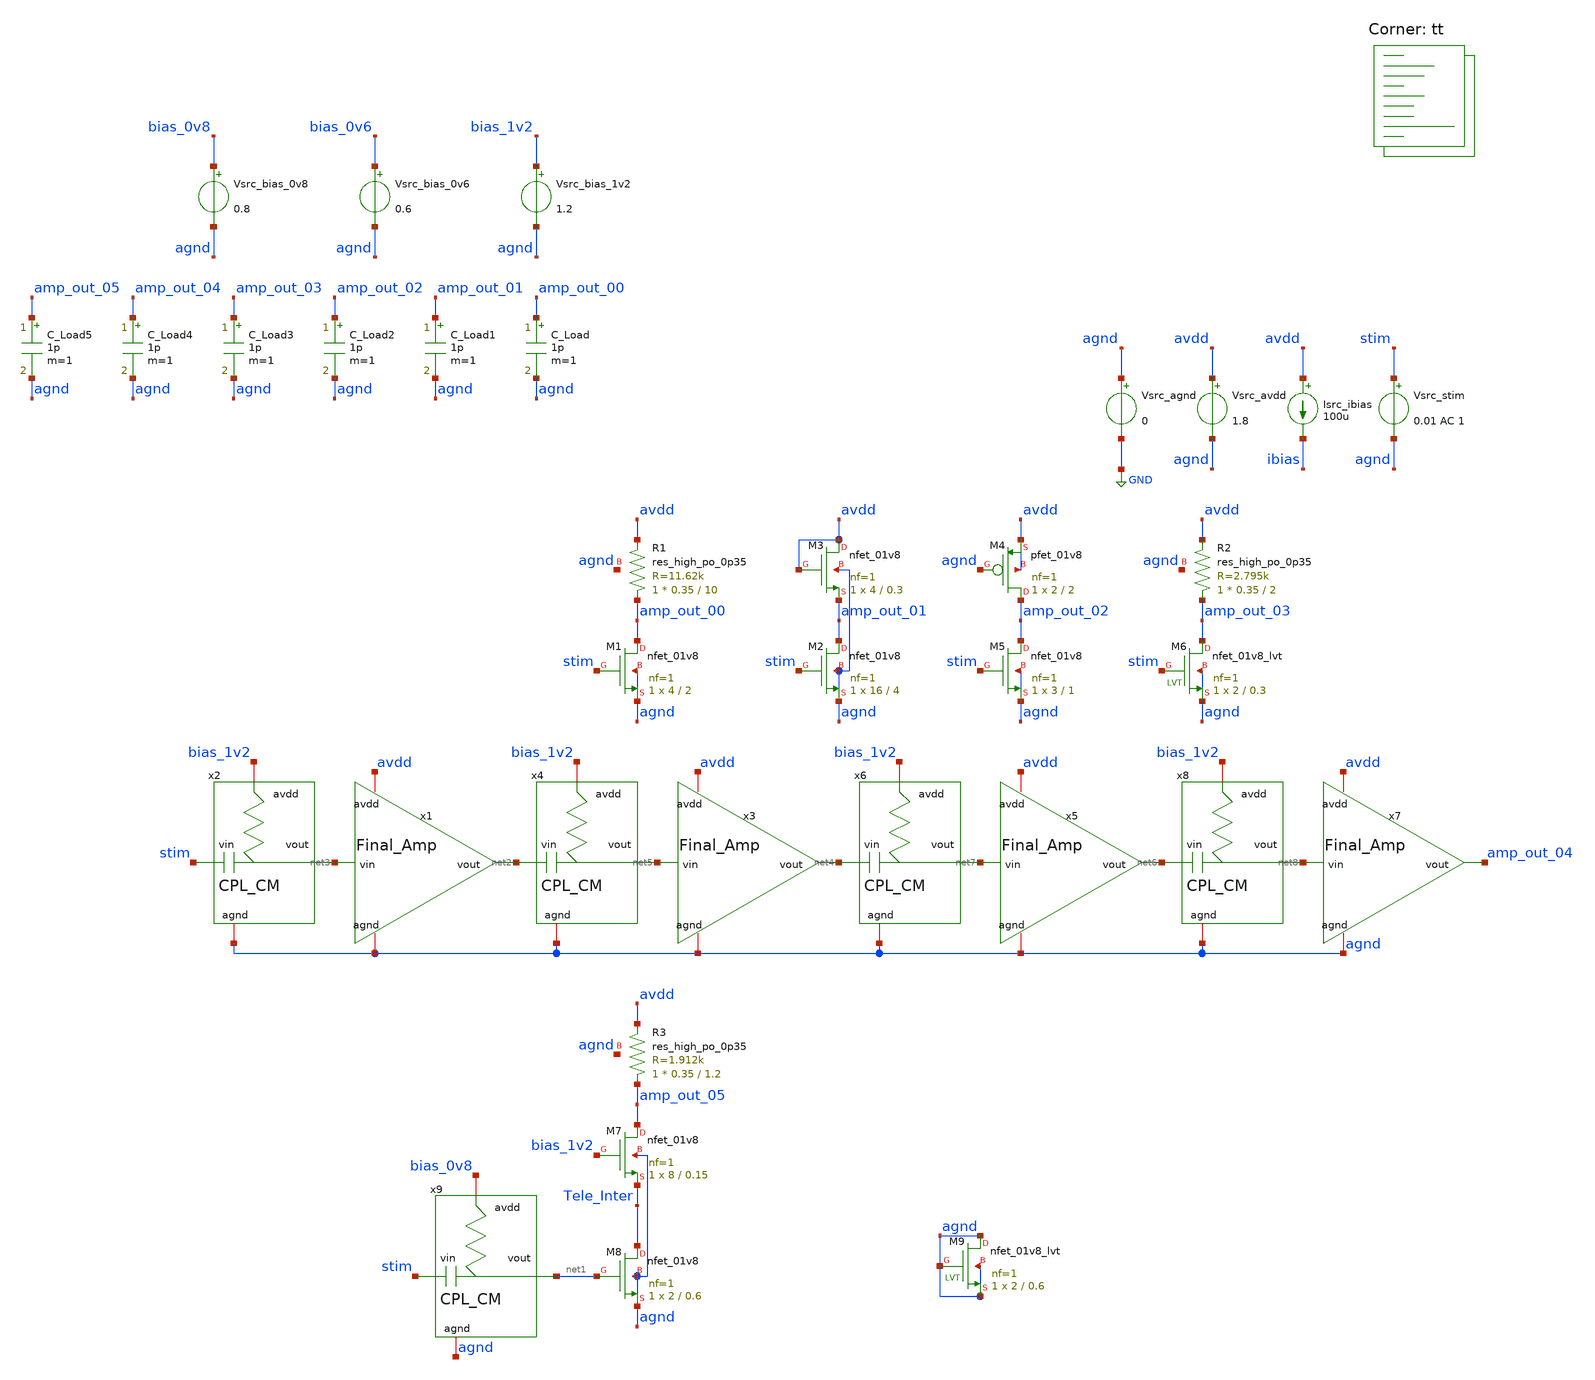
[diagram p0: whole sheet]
** sch_path: AMP/TB_Topologies.sch
**.subckt TB_Topologies
Vsrc_agnd agnd GND 0
Vsrc_avdd avdd agnd 1.8
Vsrc_stim stim agnd 0.01 AC 1
Isrc_ibias avdd ibias 100u
Vsrc_bias_1v2 bias_1v2 agnd 1.2
XM1 amp_out_00 stim agnd agnd sky130_fd_pr__nfet_01v8 L=2 W=4 nf=1 ad='int((nf+1)/2) * W/nf * 0.29' as='int((nf+2)/2) * W/nf * 0.29'
+ pd='2*int((nf+1)/2) * (W/nf + 0.29)' ps='2*int((nf+2)/2) * (W/nf + 0.29)' nrd='0.29 / W' nrs='0.29 / W'
+ sa=0 sb=0 sd=0 mult=1 m=1
XR1 amp_out_00 avdd agnd sky130_fd_pr__res_high_po_0p35 L=10 mult=1 m=1
C_Load amp_out_00 agnd 1p m=1
XM2 amp_out_01 stim agnd agnd sky130_fd_pr__nfet_01v8 L=4 W=16 nf=1 ad='int((nf+1)/2) * W/nf * 0.29'
+ as='int((nf+2)/2) * W/nf * 0.29' pd='2*int((nf+1)/2) * (W/nf + 0.29)' ps='2*int((nf+2)/2) * (W/nf + 0.29)'
+ nrd='0.29 / W' nrs='0.29 / W' sa=0 sb=0 sd=0 mult=1 m=1
XM3 avdd avdd amp_out_01 agnd sky130_fd_pr__nfet_01v8 L=0.3 W=4 nf=1 ad='int((nf+1)/2) * W/nf * 0.29'
+ as='int((nf+2)/2) * W/nf * 0.29' pd='2*int((nf+1)/2) * (W/nf + 0.29)' ps='2*int((nf+2)/2) * (W/nf + 0.29)'
+ nrd='0.29 / W' nrs='0.29 / W' sa=0 sb=0 sd=0 mult=1 m=1
C_Load1 amp_out_01 agnd 1p m=1
XM4 amp_out_02 agnd avdd avdd sky130_fd_pr__pfet_01v8 L=2 W=2 nf=1 ad='int((nf+1)/2) * W/nf * 0.29' as='int((nf+2)/2) * W/nf * 0.29'
+ pd='2*int((nf+1)/2) * (W/nf + 0.29)' ps='2*int((nf+2)/2) * (W/nf + 0.29)' nrd='0.29 / W' nrs='0.29 / W'
+ sa=0 sb=0 sd=0 mult=1 m=1
XM5 amp_out_02 stim agnd agnd sky130_fd_pr__nfet_01v8 L=1 W=3 nf=1 ad='int((nf+1)/2) * W/nf * 0.29' as='int((nf+2)/2) * W/nf * 0.29'
+ pd='2*int((nf+1)/2) * (W/nf + 0.29)' ps='2*int((nf+2)/2) * (W/nf + 0.29)' nrd='0.29 / W' nrs='0.29 / W'
+ sa=0 sb=0 sd=0 mult=1 m=1
XR2 amp_out_03 avdd agnd sky130_fd_pr__res_high_po_0p35 L=2 mult=1 m=1
XM6 amp_out_03 stim agnd agnd sky130_fd_pr__nfet_01v8_lvt L=0.3 W=2 nf=1 ad='int((nf+1)/2) * W/nf * 0.29'
+ as='int((nf+2)/2) * W/nf * 0.29' pd='2*int((nf+1)/2) * (W/nf + 0.29)' ps='2*int((nf+2)/2) * (W/nf + 0.29)'
+ nrd='0.29 / W' nrs='0.29 / W' sa=0 sb=0 sd=0 mult=1 m=1
C_Load2 amp_out_02 agnd 1p m=1
C_Load3 amp_out_03 agnd 1p m=1
x1 net2 net3 agnd avdd Final_Amp
x2 bias_1v2 agnd net3 stim CPL_CM
x3 net4 net5 agnd avdd Final_Amp
x4 bias_1v2 agnd net5 net2 CPL_CM
x5 net6 net7 agnd avdd Final_Amp
x6 bias_1v2 agnd net7 net4 CPL_CM
x7 amp_out_04 net8 agnd avdd Final_Amp
x8 bias_1v2 agnd net8 net6 CPL_CM
C_Load4 amp_out_04 agnd 1p m=1
XM7 amp_out_05 bias_1v2 Tele_Inter agnd sky130_fd_pr__nfet_01v8 L=0.15 W=8 nf=1 ad='int((nf+1)/2) * W/nf * 0.29'
+ as='int((nf+2)/2) * W/nf * 0.29' pd='2*int((nf+1)/2) * (W/nf + 0.29)' ps='2*int((nf+2)/2) * (W/nf + 0.29)'
+ nrd='0.29 / W' nrs='0.29 / W' sa=0 sb=0 sd=0 mult=1 m=1
XR3 amp_out_05 avdd agnd sky130_fd_pr__res_high_po_0p35 L=1.2 mult=1 m=1
XM8 Tele_Inter net1 agnd agnd sky130_fd_pr__nfet_01v8 L=0.6 W=2 nf=1 ad='int((nf+1)/2) * W/nf * 0.29'
+ as='int((nf+2)/2) * W/nf * 0.29' pd='2*int((nf+1)/2) * (W/nf + 0.29)' ps='2*int((nf+2)/2) * (W/nf + 0.29)'
+ nrd='0.29 / W' nrs='0.29 / W' sa=0 sb=0 sd=0 mult=1 m=1
Vsrc_bias_0v6 bias_0v6 agnd 0.6
C_Load5 amp_out_05 agnd 1p m=1
XM9 agnd agnd agnd agnd sky130_fd_pr__nfet_01v8_lvt L=0.6 W=2 nf=1 ad='int((nf+1)/2) * W/nf * 0.29' as='int((nf+2)/2) * W/nf * 0.29'
+ pd='2*int((nf+1)/2) * (W/nf + 0.29)' ps='2*int((nf+2)/2) * (W/nf + 0.29)' nrd='0.29 / W' nrs='0.29 / W'
+ sa=0 sb=0 sd=0 mult=1 m=1
x9 bias_0v8 agnd net1 stim CPL_CM
Vsrc_bias_0v8 bias_0v8 agnd 0.8
**** begin user architecture code

* this option enables mos model bin
* selection based on W/NF instead of W

.option savecurrents

.control
save all
op

* Print newline
echo

* Print stats for each MOSFET
foreach nmos xm1 xm2 xm3 xm5 x1.xm1 x3.xm1 x5.xm1 x7.xm1 xm7 xm8
 * Save stats
 save @m.{$nmos}.msky130_fd_pr__nfet_01v8[gm]
 let vth   = @m.{$nmos}.msky130_fd_pr__nfet_01v8[vth]
 let vgs   = @m.{$nmos}.msky130_fd_pr__nfet_01v8[vgs]
 let vds   = @m.{$nmos}.msky130_fd_pr__nfet_01v8[vds]
 let vdsat = @m.{$nmos}.msky130_fd_pr__nfet_01v8[vdsat]
 let gm    = @m.{$nmos}.msky130_fd_pr__nfet_01v8[gm]
 let gds   = @m.{$nmos}.msky130_fd_pr__nfet_01v8[gds]


 * Print stats
 echo Stats for $nmos:
 print vth
 print vgs
 print vds
 print vdsat
 print gm
 print gds

 * Print newline
 echo
end

foreach pmos xm4
 * Save stats
 save @m.{$pmos}.msky130_fd_pr__nfet_01v8[gm]
 let vth   = @m.{$pmos}.msky130_fd_pr__pfet_01v8[vth]
 let vgs   = @m.{$pmos}.msky130_fd_pr__pfet_01v8[vgs]
 let vds   = @m.{$pmos}.msky130_fd_pr__pfet_01v8[vds]
 let vdsat = @m.{$pmos}.msky130_fd_pr__pfet_01v8[vdsat]
 let gm    = @m.{$pmos}.msky130_fd_pr__pfet_01v8[gm]
 let gds   = @m.{$pmos}.msky130_fd_pr__pfet_01v8[gds]

 * Print stats
 echo Stats for $pmos:
 print vth
 print vgs
 print vds
 print vdsat
 print gm
 print gds

 * Print newline
 echo
end

foreach nmos_lvt xm6 xm9
 * Save stats
 save @m.{$nmos}.msky130_fd_pr__nfet_01v8_lvt[gm]
 let vth   = @m.{$nmos_lvt}.msky130_fd_pr__nfet_01v8_lvt[vth]
 let vgs   = @m.{$nmos_lvt}.msky130_fd_pr__nfet_01v8_lvt[vgs]
 let vds   = @m.{$nmos_lvt}.msky130_fd_pr__nfet_01v8_lvt[vds]
 let vdsat = @m.{$nmos_lvt}.msky130_fd_pr__nfet_01v8_lvt[vdsat]
 let gm    = @m.{$nmos_lvt}.msky130_fd_pr__nfet_01v8_lvt[gm]
 let gds   = @m.{$nmos_lvt}.msky130_fd_pr__nfet_01v8_lvt[gds]


 * Print stats
 echo Stats for $nmos_lvt:
 print vth
 print vgs
 print vds
 print vdsat
 print gm
 print gds

 * Print newline
 echo
end

* Print region of operation
echo Regions of Operation:
foreach nmos xm1 xm2 xm3 xm5 x1.xm1 x3.xm1 x5.xm1 x7.xm1 xm7 xm8
 * Save stats
 let vds = @m.{$nmos}.msky130_fd_pr__nfet_01v8[vds]
 let vgs = @m.{$nmos}.msky130_fd_pr__nfet_01v8[vgs]
 let vth = @m.{$nmos}.msky130_fd_pr__nfet_01v8[vth]

 * Check and print regions
 if (vgs <= vth)
  echo $nmos: N Cutoff
  print vgs
  print vth
 end
 if (vgs > vth) & (vds <= (vgs - vth))
  echo $nmos: N Triode
  print vgs
  print vth
  print vds
 end
 if (vgs > vth) & (vds > (vgs - vth))
  echo $nmos: N Saturation
 end
end

foreach pmos xm4
 * Save stats
 let vds = @m.{$pmos}.msky130_fd_pr__pfet_01v8[vds]
 let vgs = @m.{$pmos}.msky130_fd_pr__pfet_01v8[vgs]
 let vth = @m.{$pmos}.msky130_fd_pr__pfet_01v8[vth]

 * Check and print regions
 if (abs(vgs) <= abs(vth))
  echo $pmos: P Cutoff
  print vgs
  print vth
 end
 if (abs(vgs) > abs(vth)) & (abs(vds) <= (abs(vgs) - abs(vth)))
  echo $pmos: P Triode
  print vgs
  print vth
  print vds
 end
 if (abs(vgs) > abs(vth)) & (abs(vds) > (abs(vgs) - abs(vth)))
  echo $pmos: P Saturation
 end
end

* Print region of operation
foreach nmos_lvt xm6 xm9
 * Save stats
 let vds = @m.{$nmos_lvt}.msky130_fd_pr__nfet_01v8_lvt[vds]
 let vgs = @m.{$nmos_lvt}.msky130_fd_pr__nfet_01v8_lvt[vgs]
 let vth = @m.{$nmos_lvt}.msky130_fd_pr__nfet_01v8_lvt[vth]

 * Check and print regions
 if (vgs <= vth)
  echo $nmos_lvt: N Cutoff
  print vgs
  print vth
 end
 if (vgs > vth) & (vds <= (vgs - vth))
  echo $nmos_lvt: N Triode
  print vgs
  print vth
  print vds
 end
 if (vgs > vth) & (vds > (vgs - vth))
  echo $nmos_lvt: N Saturation
 end
end

* Print newline
echo

* Sweep frequency
write TB_Topologies.raw
set appendwrite
ac dec 100 1 1e11
remzerovec

* Calculate gain
let ratio_00 = v(amp_out_00)/v(stim)
let ratio_01 = v(amp_out_01)/v(stim)
let ratio_02 = v(amp_out_02)/v(stim)
let ratio_03 = v(amp_out_03)/v(stim)
let ratio_04 = v(amp_out_04)/v(stim)
let ratio_05 = v(amp_out_05)/v(stim)

let gain_00 = db(mag(ratio_00))
let gain_01 = db(mag(ratio_01))
let gain_02 = db(mag(ratio_02))
let gain_03 = db(mag(ratio_03))
let gain_04 = db(mag(ratio_04))
let gain_05 = db(mag(ratio_05))

write TB_Topologies.raw

.endc


.lib $::SKYWATER_MODELS/sky130.lib.spice tt
**** end user architecture code
**.ends
.GLOBAL GND
.end
